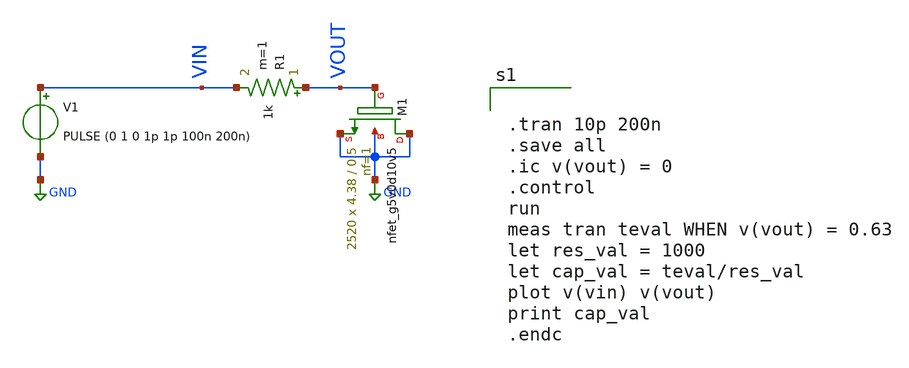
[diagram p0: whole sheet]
** sch_path: xschem/TB_hvNMOS_cgate_ext_SKY130.sch
.lib $::SKYWATER_MODELS/sky130.lib.spice tt
.include $::SKYWATER_STDCELLS/sky130_fd_sc_hd.spice

**.subckt TB_hvNMOS_cgate_ext_SKY130
R1 VOUT VIN 1k m=1
V1 VIN GND PULSE (0 1 0 1p 1p 100n 200n)
XM1 GND VOUT GND GND sky130_fd_pr__nfet_g5v0d10v5 L=0.5 W=4.38 nf=1 ad='int((nf+1)/2) * W/nf * 0.29'
+ as='int((nf+2)/2) * W/nf * 0.29' pd='2*int((nf+1)/2) * (W/nf + 0.29)' ps='2*int((nf+2)/2) * (W/nf + 0.29)'
+ nrd='0.29 / W' nrs='0.29 / W' sa=0 sb=0 sd=0 mult=2520 m=2520
**** begin user architecture code


.tran 10p 200n
.save all
.ic v(vout) = 0
.control
run
meas tran teval WHEN v(vout) = 0.63
let res_val = 1000
let cap_val = teval/res_val
plot v(vin) v(vout)
print cap_val
.endc




.param temp=27

.param mult_M2 = 1200
.param w_M2 =10u
*.param l_M2 =0.25u
.param l_M2 =0.25u
.param ng_M2 =1





**** end user architecture code
**.ends
.GLOBAL GND
.end
